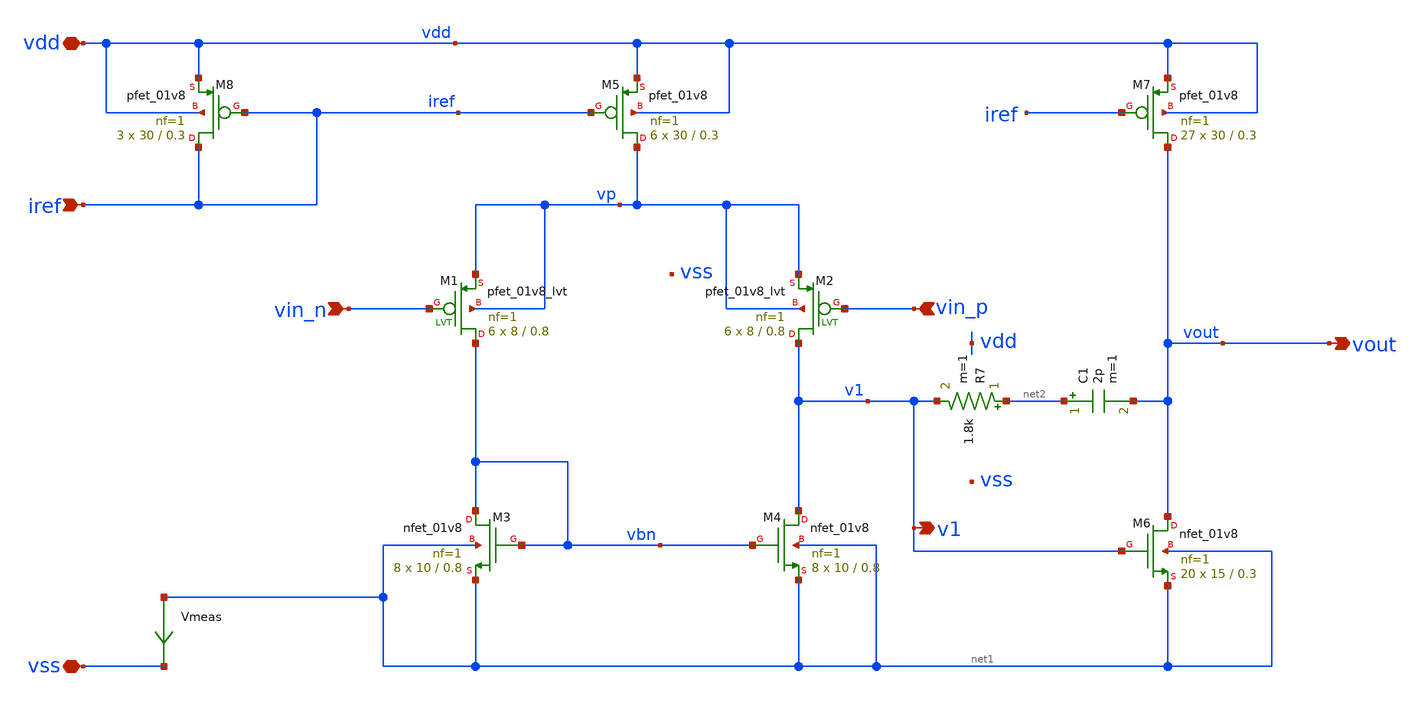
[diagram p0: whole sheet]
** sch_path: opamp/opamp.sch
**.subckt opamp vdd vss vin_n vin_p iref vout v1
*.iopin vdd
*.iopin vss
*.ipin vin_n
*.ipin vin_p
*.ipin iref
*.opin vout
*.opin v1
XM3 vbn vbn net1 net1 sky130_fd_pr__nfet_01v8 L=0.8 W=10 nf=1 ad='int((1 + 1)/2) * 10 / 1 * 0.29' as='W * 0.29'
+ pd='2 * (W + 0.29)' ps='2 * (W + 0.29)' nrd='0.29 / W' nrs='0.29 / W' sa=0 sb=0 sd=0 mult=8 m=8
XM4 v1 vbn net1 net1 sky130_fd_pr__nfet_01v8 L=0.8 W=10 nf=1 ad='int((1 + 1)/2) * 10 / 1 * 0.29' as='W * 0.29'
+ pd='2 * (W + 0.29)' ps='2 * (W + 0.29)' nrd='0.29 / W' nrs='0.29 / W' sa=0 sb=0 sd=0 mult=8 m=8
XM5 vp iref vdd vdd sky130_fd_pr__pfet_01v8 L=0.3 W=30 nf=1 ad='W * 0.29' as='W * 0.29' pd='2 * (W + 0.29)'
+ ps='2 * (W + 0.29)' nrd='0.29 / W' nrs='0.29 / W' sa=0 sb=0 sd=0 mult=6 m=6
XqM7 vout iref vdd vdd sky130_fd_pr__pfet_01v8 L=0.3 W=30 nf=1 ad='W * 0.29' as='W * 0.29' pd='2 * (W + 0.29)'
+ ps='2 * (W + 0.29)' nrd='0.29 / W' nrs='0.29 / W' sa=0 sb=0 sd=0 mult=27 m=27
XM8 iref iref vdd vdd sky130_fd_pr__pfet_01v8 L=0.3 W=30 nf=1 ad='W * 0.29' as='W * 0.29' pd='2 * (W + 0.29)'
+ ps='2 * (W + 0.29)' nrd='0.29 / W' nrs='0.29 / W' sa=0 sb=0 sd=0 mult=3 m=3
XM1 vbn vin_n vp vp sky130_fd_pr__pfet_01v8_lvt L=0.8 W=8 nf=1 ad='int((nf+1)/2) * W/nf * 0.29' as='int((nf+2)/2) * W/nf * 0.29'
+ pd='2*int((nf+1)/2) * (W/nf + 0.29)' ps='2*int((nf+2)/2) * (W/nf + 0.29)' nrd='0.29 / W' nrs='0.29 / W'
+ sa=0 sb=0 sd=0 mult=6 m=6
XM2 v1 vin_p vp vp sky130_fd_pr__pfet_01v8_lvt L=0.8 W=8 nf=1 ad='int((nf+1)/2) * W/nf * 0.29' as='int((nf+2)/2) * W/nf * 0.29'
+ pd='2*int((nf+1)/2) * (W/nf + 0.29)' ps='2*int((nf+2)/2) * (W/nf + 0.29)' nrd='0.29 / W' nrs='0.29 / W'
+ sa=0 sb=0 sd=0 mult=6 m=6
C1 net2 vout 2p m=1
Vmeas net1 vss 0
.save i(vmeas)
R7 net2 v1 1.8k m=1
XM6 vout v1 net1 net1 sky130_fd_pr__nfet_01v8 L=0.3 W=15 nf=1 ad='W * 0.29' as='W * 0.29' pd='2 * (W + 0.29)'
+ ps='2 * (W + 0.29)' nrd='0.29 / W' nrs='0.29 / W' sa=0 sb=0 sd=0 mult=20 m=20
**.ends
.end
